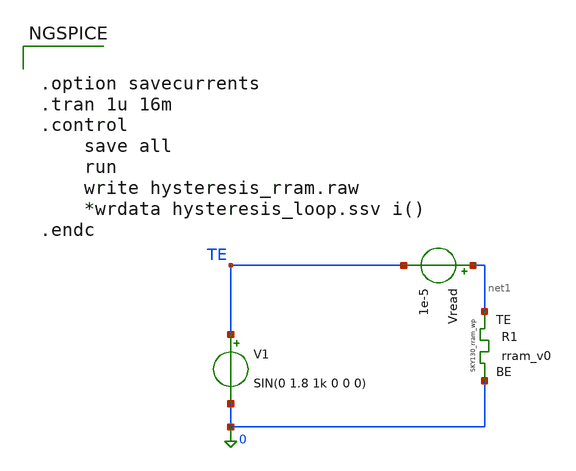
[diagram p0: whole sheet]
** sch_path: Ricardo/STDP_test/hysteresis_rram.sch
**.subckt hysteresis_rram
XR1 net1 0 rram_v0
V1 TE 0 SIN(0 1.8 1k 0 0 0)
Vread net1 TE 1e-5
**** begin user architecture code

** opencircuitdesign pdks install
.inc $::SKYWATER_MODELS/rram_v0.spice



.option savecurrents
.tran 1u 16m
.control
	save all
	run
	write hysteresis_rram.raw
	*wrdata hysteresis_loop.ssv i()
.endc



**** end user architecture code
**.ends
.end
